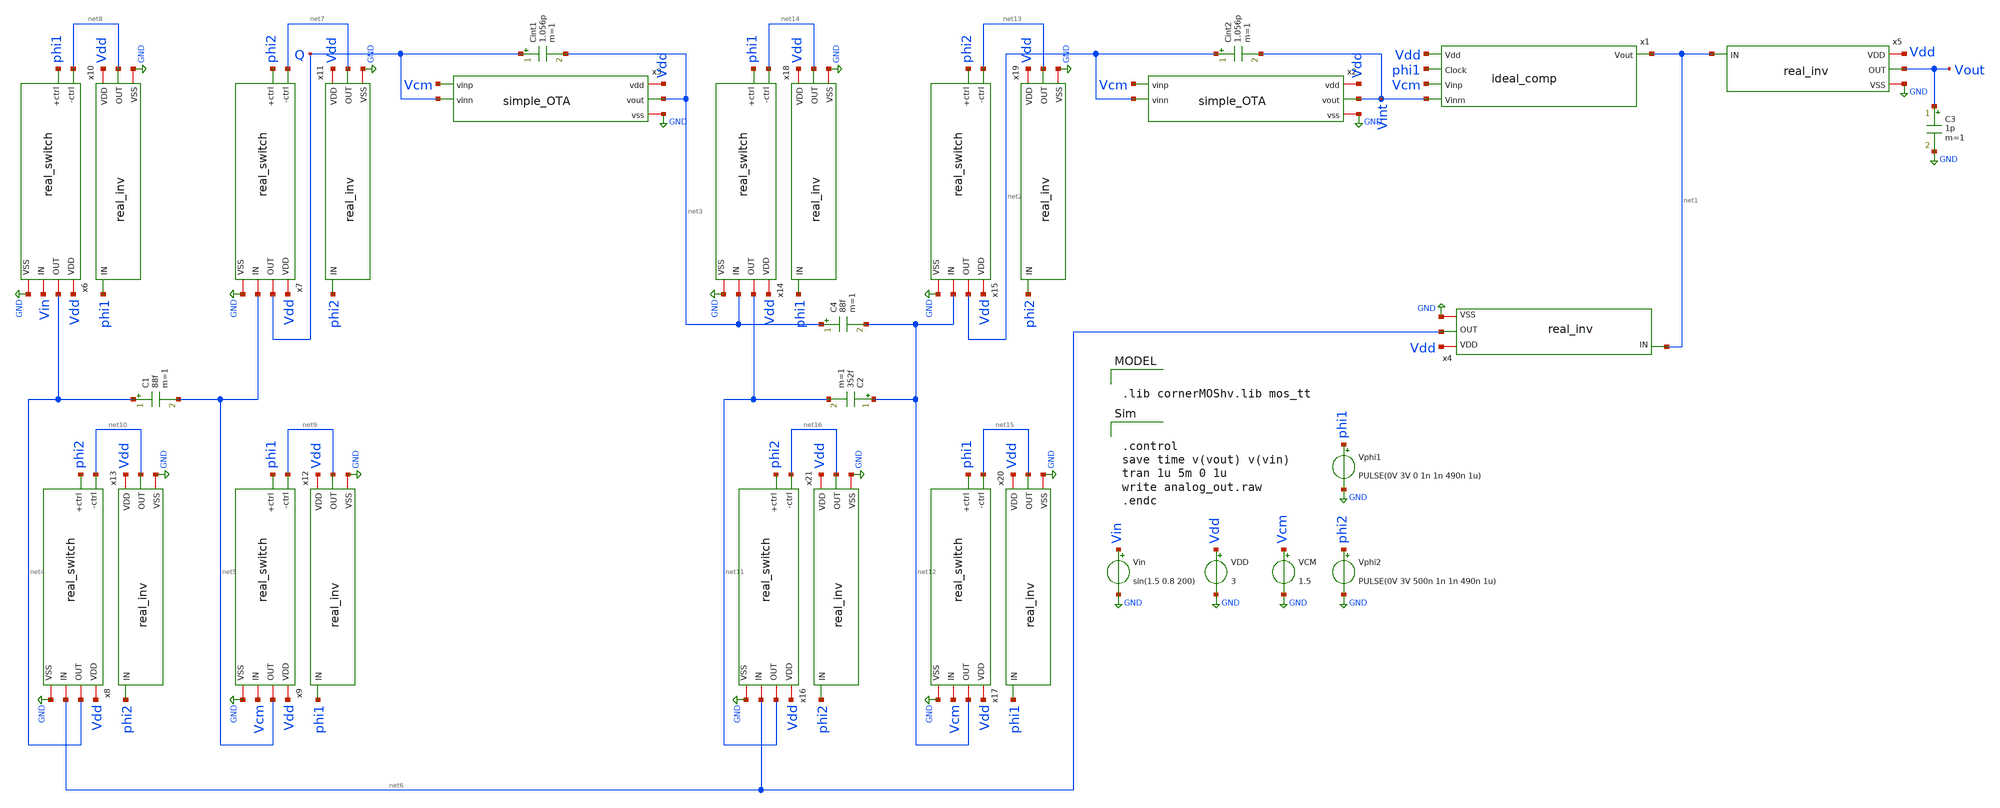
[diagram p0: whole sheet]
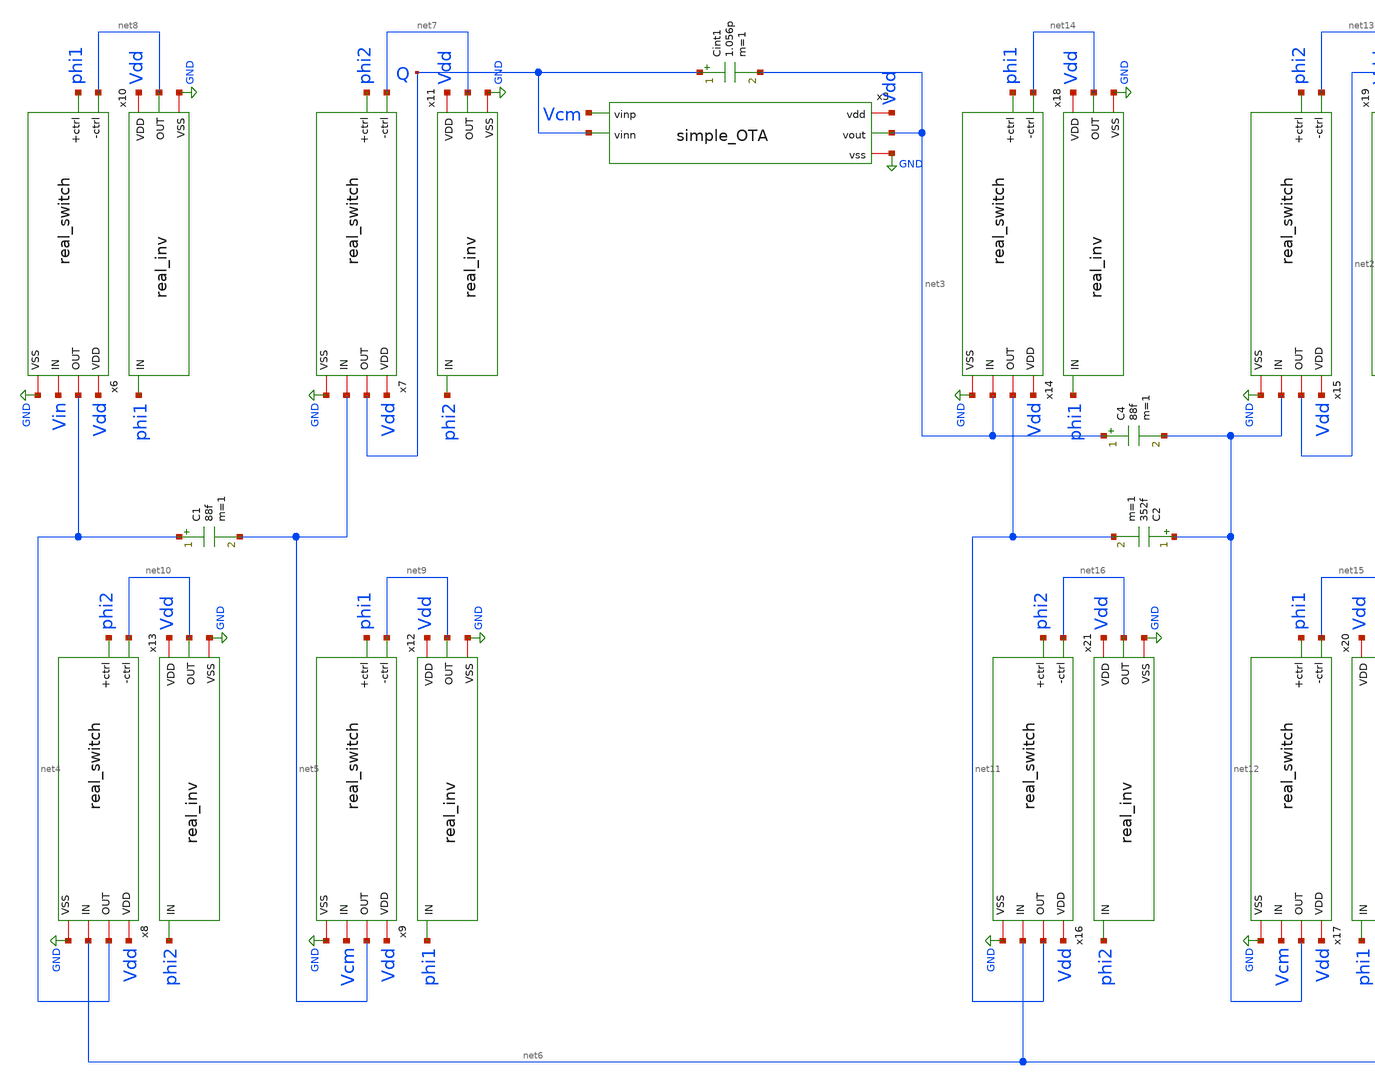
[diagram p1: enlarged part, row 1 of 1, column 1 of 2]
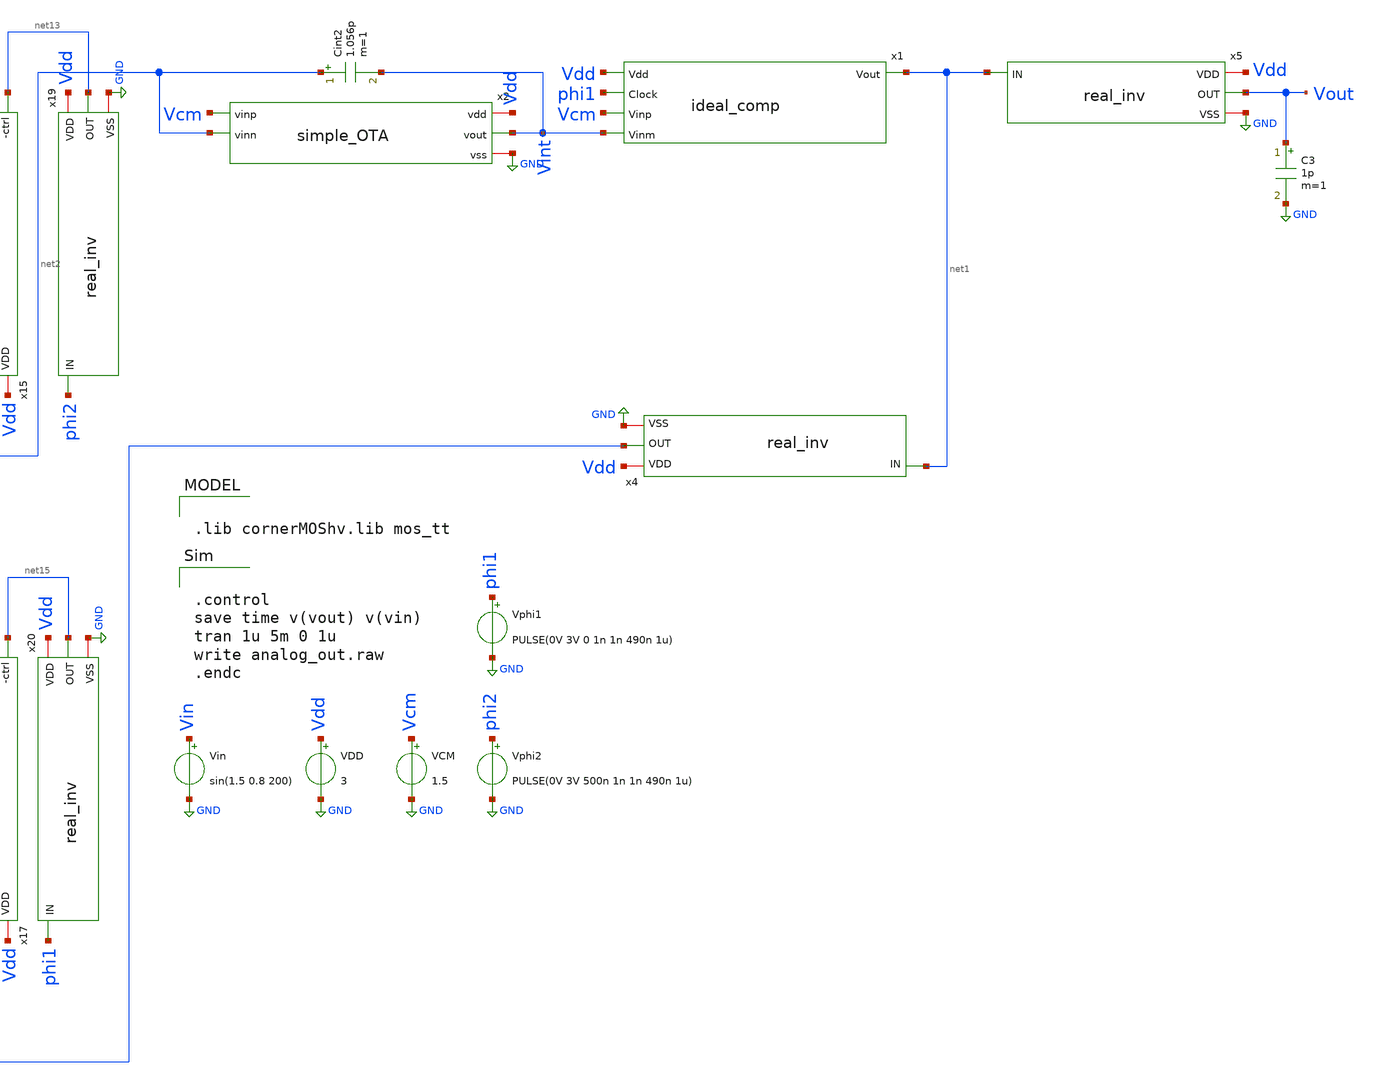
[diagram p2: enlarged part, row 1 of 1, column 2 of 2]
** sch_path: real_circuit/sandbox/circuit.sch
**.subckt circuit
VDD Vdd GND 3
VCM Vcm GND 1.5
Vin Vin GND sin(1.5 0.8 200)
Vphi1 phi1 GND PULSE(0V 3V 0 1n 1n 490n 1u)
Vphi2 phi2 GND PULSE(0V 3V 500n 1n 1n 490n 1u)
C2 net12 net11 352f m=1
Cint2 net2 Vint 1.056p m=1
C1 net4 net5 88f m=1
Cint1 Q net3 1.056p m=1
x1 net1 Vdd phi1 Vcm Vint ideal_comp
x4 Vdd net1 net6 GND real_inv
x5 Vdd net1 Vout GND real_inv
x6 net8 Vdd net4 Vin phi1 GND real_switch
x7 net7 Vdd Q net5 phi2 GND real_switch
x8 net10 Vdd net4 net6 phi2 GND real_switch
x9 net9 Vdd net5 Vcm phi1 GND real_switch
x10 Vdd phi1 net8 GND real_inv
x11 Vdd phi2 net7 GND real_inv
x12 Vdd phi1 net9 GND real_inv
x13 Vdd phi2 net10 GND real_inv
x14 net14 Vdd net11 net3 phi1 GND real_switch
x15 net13 Vdd net2 net12 phi2 GND real_switch
x16 net16 Vdd net11 net6 phi2 GND real_switch
x17 net15 Vdd net12 Vcm phi1 GND real_switch
x18 Vdd phi1 net14 GND real_inv
x19 Vdd phi2 net13 GND real_inv
x20 Vdd phi1 net15 GND real_inv
x21 Vdd phi2 net16 GND real_inv
C3 Vout GND 1p m=1
x2 Vdd Vint Vcm net2 GND simple_OTA
x3 Vdd net3 Vcm Q GND simple_OTA
C4 net3 net12 88f m=1
**** begin user architecture code


.control
save time v(vout) v(vin)
tran 1u 5m 0 1u
write analog_out.raw
.endc



.lib cornerMOShv.lib mos_tt

**** end user architecture code
**.ends
.GLOBAL GND
.end
